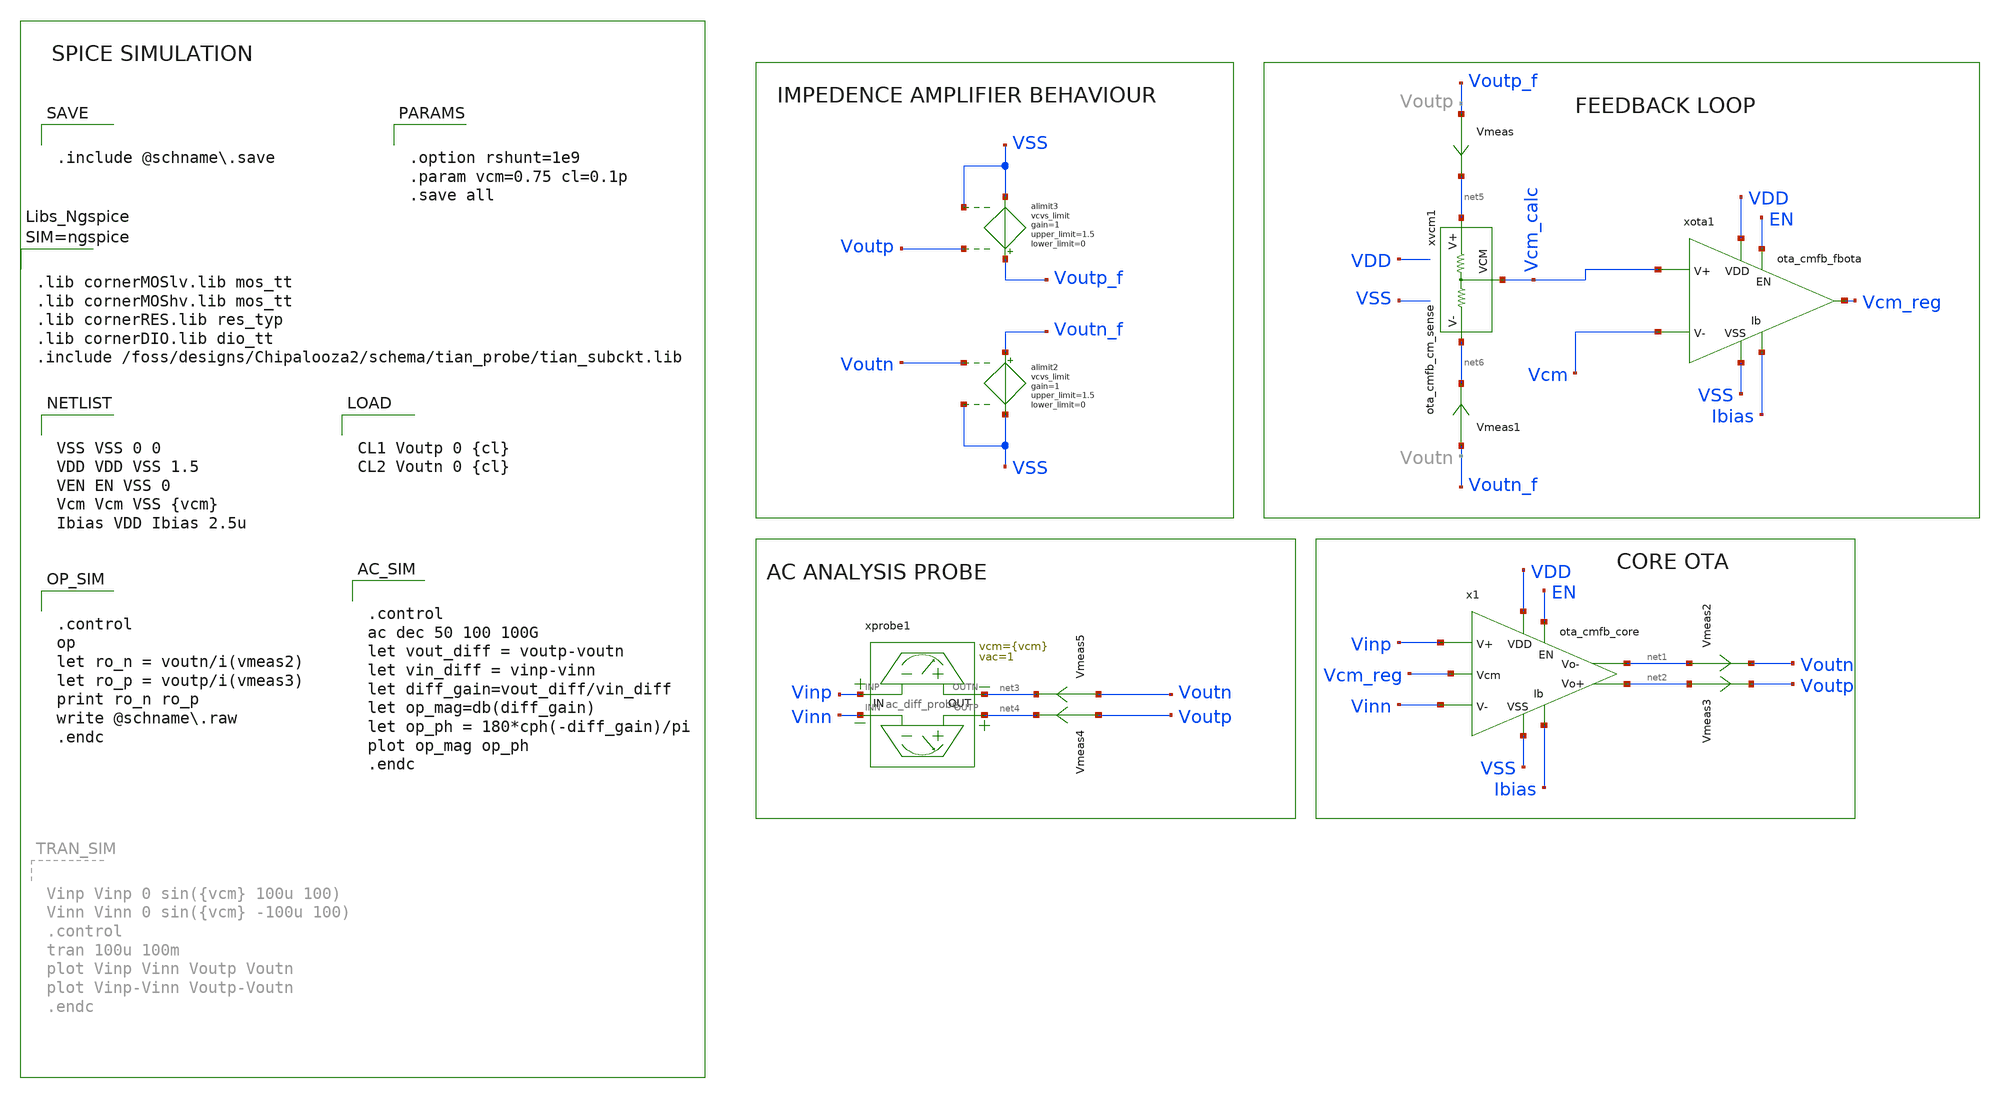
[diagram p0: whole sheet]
** sch_path: schema/ota_cmfb/ota_cmfb_tb.sch
**.subckt ota_cmfb_tb
x1 VDD Vcm_reg Vinn Vinp Ibias net1 net2 VSS EN ota_cmfb_core
xprobe1 Vinp net3 Vinn net4 ac_diff_probe vcm={vcm} vac=1
xvcm1 net5 net6 Vcm_calc ota_cmfb_cm_sense
alimit2 %vd( Voutn VSS ) %vd( Voutn_f VSS ) alimit2
.model alimit2 limit ( gain=1 out_lower_limit=0 out_upper_limit=1.5 )
alimit3 %vd( Voutp VSS ) %vd( Voutp_f VSS ) alimit3
.model alimit3 limit ( gain=1 out_lower_limit=0 out_upper_limit=1.5 )
Vmeas Voutp_f net5 0
.save i(vmeas)
Vmeas1 Voutn_f net6 0
.save i(vmeas1)
xota1 VDD EN Ibias Vcm Vcm_calc Vcm_reg VSS ota_cmfb_fbota
Vmeas2 net1 Voutn 0
.save i(vmeas2)
Vmeas3 net2 Voutp 0
.save i(vmeas3)
Vmeas4 Voutp net4 0
.save i(vmeas4)
Vmeas5 Voutn net3 0
.save i(vmeas5)
**** begin user architecture code


VSS VSS 0 0
VDD VDD VSS 1.5
VEN EN VSS 0
Vcm Vcm VSS {vcm}
Ibias VDD Ibias 2.5u



.control
op
let ro_n = voutn/i(vmeas2)
let ro_p = voutp/i(vmeas3)
print ro_n ro_p
write @schname.raw
.endc




.lib cornerMOSlv.lib mos_tt
.lib cornerMOShv.lib mos_tt
.lib cornerRES.lib res_typ
.lib cornerDIO.lib dio_tt
.include /foss/designs/Chipalooza2/schema/tian_probe/tian_subckt.lib





.control
ac dec 50 100 100G
let vout_diff = voutp-voutn
let vin_diff = vinp-vinn
let diff_gain=vout_diff/vin_diff
let op_mag=db(diff_gain)
let op_ph = 180*cph(-diff_gain)/pi
plot op_mag op_ph
.endc




.option rshunt=1e9
.param vcm=0.75 cl=0.1p
.save all




CL1 Voutp 0 {cl}
CL2 Voutn 0 {cl}



.include @schname.save

fill=0
**** end user architecture code
**.ends

* expanding   symbol:  /foss/designs/Chipalooza2/schema/ota_cmfb_core/ota_cmfb_core.sym # of pins=9
** sym_path: schema/ota_cmfb_core/ota_cmfb_core.sym
** sch_path: schema/ota_cmfb_core/ota_cmfb_core.sch
.subckt ota_cmfb_core VDD Vcm_reg Vinn Vinp Ibias Voutn Voutp VSS EN
*.opin Voutn
*.opin Voutp
*.iopin VDD
*.iopin VSS
*.ipin Vinp
*.ipin Ibias
*.ipin Vinn
*.ipin Vcm_reg
*.ipin EN
XM1 Voutp Ibias VSS VSS sg13_lv_nmos w=0.5u l=10u ng=1 m=4 mm_ok=1
XM2 net1 Vinn Voutp VDD sg13_lv_pmos w=2.5u l=2u ng=1 m=8 mm_ok=1
XM3 Voutn Ibias VSS VSS sg13_lv_nmos w=0.5u l=10u ng=1 m=4 mm_ok=1
XM4 net1 Vinp Voutn VDD sg13_lv_pmos w=2.5u l=2u ng=1 m=8 mm_ok=1
XM5 VDD Vcm_reg net1 VDD sg13_lv_pmos w=2.5u l=5u ng=1 m=4 mm_ok=1
XM6 Ibias Ibias VSS VSS sg13_lv_nmos w=0.5u l=10u ng=1 m=1 mm_ok=1
XM7 Ibias EN VSS VSS sg13_lv_nmos w=0.15u l=0.13u ng=1 m=1 mm_ok=1
.ends


* expanding   symbol:  /foss/designs/Chipalooza2/schema/ac_diff_probe/ac_diff_probe.sym # of pins=4
** sym_path: schema/ac_diff_probe/ac_diff_probe.sym
** sch_path: schema/ac_diff_probe/ac_diff_probe.sch
.subckt ac_diff_probe INP OUTN INN OUTP  vcm=0.75 vac=0.1
*.iopin OUTN
*.iopin INP
*.iopin OUTP
*.iopin INN
xprobe1 OUTN INP ac_probe vcm={vcm} vac={vac}
xprobe2 OUTP INN ac_probe vcm={vcm} vac=-{vac}
.ends


* expanding   symbol:  /foss/designs/Chipalooza2/schema/ota_cmfb_cm_sense/ota_cmfb_cm_sense.sym # of
*+ pins=3
** sym_path: schema/ota_cmfb_cm_sense/ota_cmfb_cm_sense.sym
** sch_path: schema/ota_cmfb_cm_sense/ota_cmfb_cm_sense.sch
.subckt ota_cmfb_cm_sense Voutp Voutn VCM
*.ipin Voutp
*.ipin Voutn
*.opin VCM
XR1 Voutn VCM 0 rhigh w=0.5e-6 l=1e-6*10 m=1 b=0 mm_ok=1
XR2 Voutp VCM 0 rhigh w=0.5e-6 l=1e-6*10 m=1 b=0 mm_ok=1
.ends


* expanding   symbol:  /foss/designs/Chipalooza2/schema/ota_cmfb_fbota/ota_cmfb_fbota.sym # of
*+ pins=7
** sym_path: schema/ota_cmfb_fbota/ota_cmfb_fbota.sym
** sch_path: schema/ota_cmfb_fbota/ota_cmfb_fbota.sch
.subckt ota_cmfb_fbota VDD EN Ibias Vinn Vinp Vout VSS
*.opin Vout
*.iopin VDD
*.iopin VSS
*.ipin Vinp
*.ipin Ibias
*.ipin Vinn
*.ipin EN
XM1 Vout mirror VSS VSS sg13_lv_nmos w=0.5u l=10u ng=1 m=2 mm_ok=1
XM2 net1 Vinn Vout VDD sg13_lv_pmos w=2.5u l=1u ng=1 m=2 mm_ok=1
XM3 mirror mirror VSS VSS sg13_lv_nmos w=0.5u l=10u ng=1 m=2 mm_ok=1
XM4 net1 Vinp mirror VDD sg13_lv_pmos w=2.5u l=1u ng=1 m=2 mm_ok=1
XM5 VDD tail_bias net1 VDD sg13_lv_pmos w=2.5u l=5u ng=1 m=4 mm_ok=1
XM7 mirror EN VSS VSS sg13_lv_nmos w=0.15u l=0.13u ng=1 m=1 mm_ok=1
XM8 VDD tail_bias tail_bias VDD sg13_lv_pmos w=2.5u l=5u ng=1 m=1 mm_ok=1
XM9 tail_bias Ibias VSS VSS sg13_lv_nmos w=0.5u l=10u ng=1 m=1 mm_ok=1
.ends


* expanding   symbol:  /foss/designs/Chipalooza2/schema/ac_probe/ac_probe.sym # of pins=2
** sym_path: schema/ac_probe/ac_probe.sym
** sch_path: schema/ac_probe/ac_probe.sch
.subckt ac_probe OUT IN  vcm=0.75 vac=0.01

*.iopin IN
*.iopin OUT
C1 net1 IN 1 m=1
V1 net1 0 {vcm} ac {vac}
L1 OUT net2 1G m=1
R1 net2 IN 1m m=1
.ends

.end
